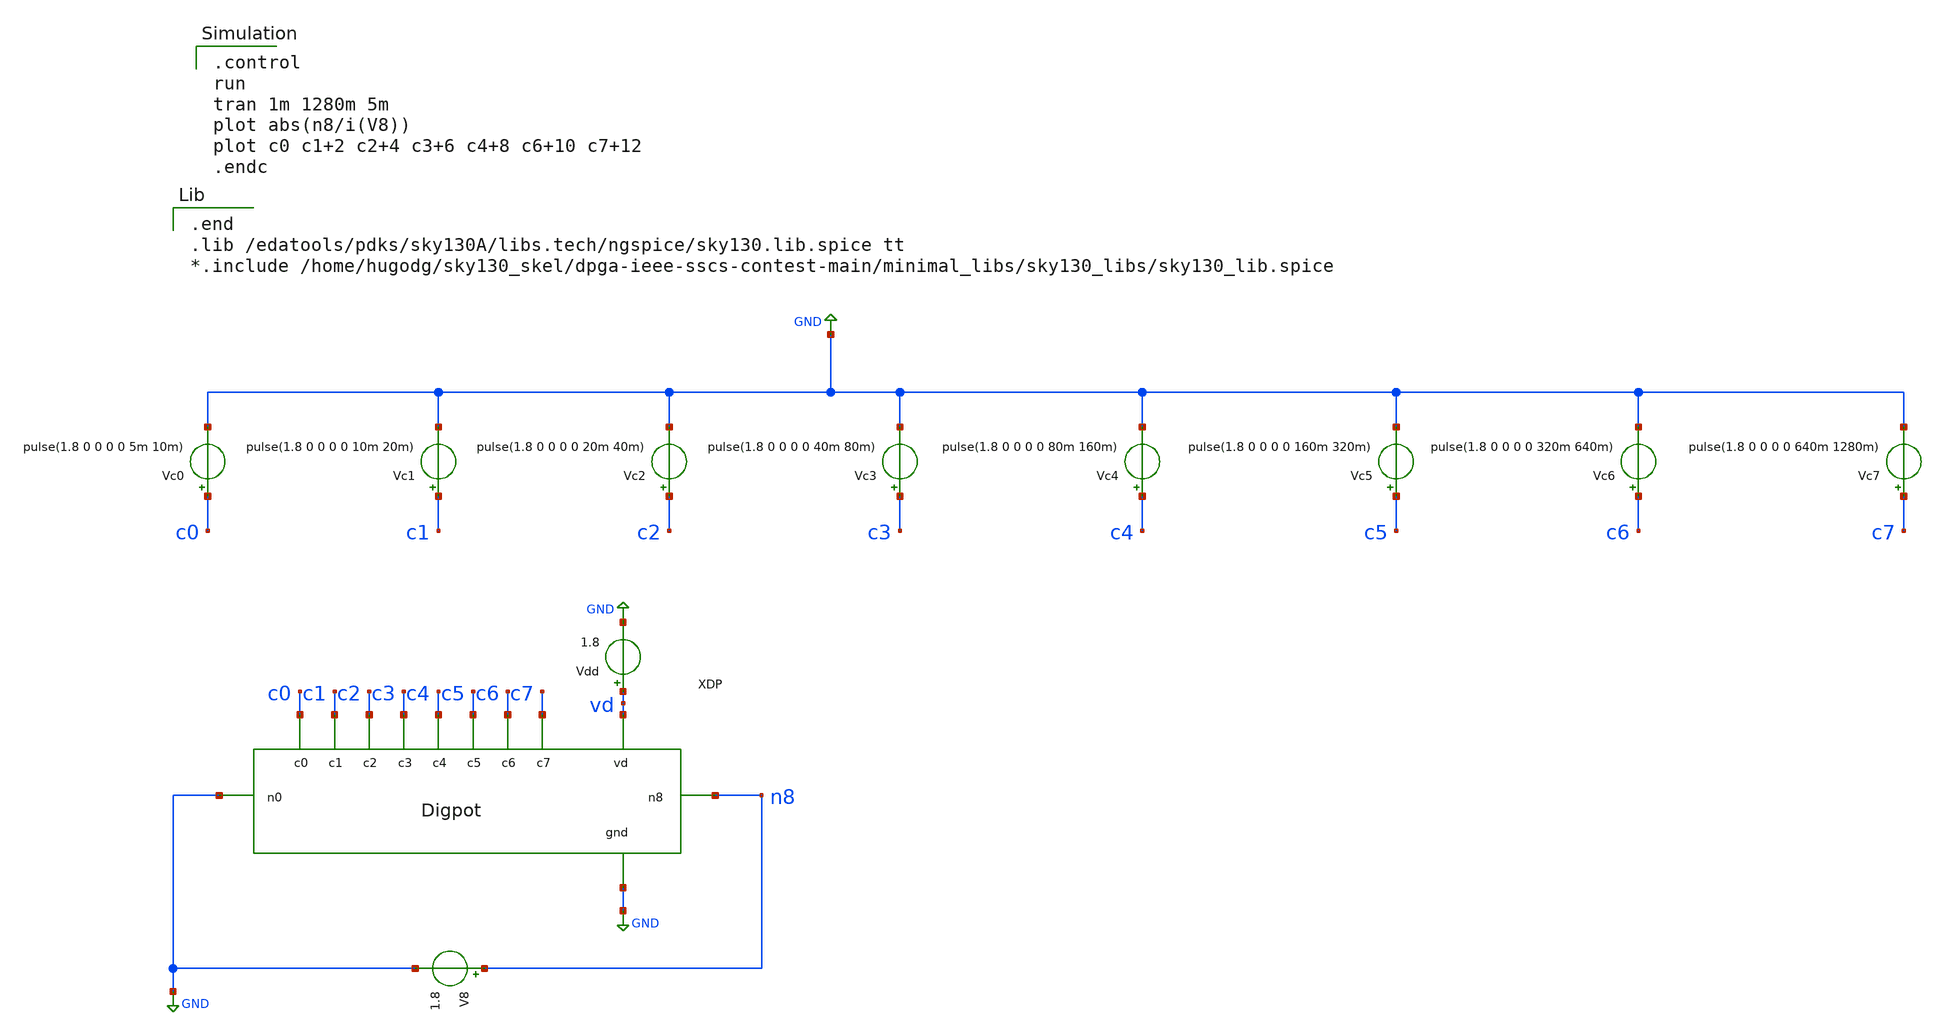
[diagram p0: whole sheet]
** sch_path: xschem/digpot-tb.sch
**.subckt digpot-tb
x1 GND vd c5 c1 c2 c6 c7 c3 c0 c4 n8 GND digpot
V8 n8 GND 1.8
Vdd vd GND 1.8
Vc0 c0 GND pulse(1.8 0 0 0 0 5m 10m)
Vc1 c1 GND pulse(1.8 0 0 0 0 10m 20m)
Vc2 c2 GND pulse(1.8 0 0 0 0 20m 40m)
Vc3 c3 GND pulse(1.8 0 0 0 0 40m 80m)
Vc4 c4 GND pulse(1.8 0 0 0 0 80m 160m)
Vc5 c5 GND pulse(1.8 0 0 0 0 160m 320m)
Vc6 c6 GND pulse(1.8 0 0 0 0 320m 640m)
Vc7 c7 GND pulse(1.8 0 0 0 0 640m 1280m)
**** begin user architecture code

.end
.lib /edatools/pdks/sky130A/libs.tech/ngspice/sky130.lib.spice tt
*.include /home/hugodg/sky130_skel/dpga-ieee-sscs-contest-main/minimal_libs/sky130_libs/sky130_lib.spice


.control
run
tran 1m 1280m 5m
plot abs(n8/i(V8))
plot c0 c1+2 c2+4 c3+6 c4+8 c6+10 c7+12
.endc

**** end user architecture code
**.ends

* expanding   symbol:  /home/hugodg/sky130_skel/dpga-ieee-sscs-contest-main/xschem/digpot.sym # of
*+ pins=12
** sym_path: xschem/digpot.sym
** sch_path: xschem/digpot.sch
.subckt digpot gnd vd c5 c1 c2 c6 c7 c3 c0 c4 n8 n0
*.ipin c0
*.ipin c1
*.ipin c2
*.ipin c3
*.ipin c4
*.ipin c5
*.ipin c6
*.ipin c7
*.iopin gnd
*.iopin vd
*.iopin n0
*.iopin n8
xtg1 c0 vd n1 gnd n0 tg
xtg2 c1 vd n2 gnd n1 tg
xtg3 c2 vd n3 gnd n2 tg
xtg4 c3 vd n4 gnd n3 tg
xtg5 c4 vd n5 gnd n4 tg
xtg6 c5 vd n6 gnd n5 tg
xtg7 c6 vd n7 gnd n6 tg
xtg8 c7 vd n8 gnd n7 tg
XR0 n1 n0 gnd sky130_fd_pr__res_high_po_0p35 L=0.98 mult=1 m=1
XR1 n2 n1 gnd sky130_fd_pr__res_high_po_0p35 L=2.07 mult=1 m=1
XR2 n3 n2 gnd sky130_fd_pr__res_xhigh_po_0p35 L=0.58 mult=1 m=1
XR3 n4 n3 gnd sky130_fd_pr__res_xhigh_po_0p35 L=1.28 mult=1 m=1
XR4 n5 n4 gnd sky130_fd_pr__res_xhigh_po_0p35 L=2.68 mult=1 m=1
XR5 n6 n5 gnd sky130_fd_pr__res_xhigh_po_0p35 L=5.48 mult=1 m=1
XR6 n7 n6 gnd sky130_fd_pr__res_xhigh_po_0p35 L=10.73 mult=1 m=1
XR7 n8 n7 gnd sky130_fd_pr__res_xhigh_po_0p35 L=22.28 mult=1 m=1
.ends


* expanding   symbol:  /home/hugodg/sky130_skel/dpga-ieee-sscs-contest-main/xschem/tg.sym # of
*+ pins=5
** sym_path: xschem/tg.sym
** sch_path: xschem/tg.sch
.subckt tg ctrl vd b vgnd a
*.iopin vd
*.iopin vgnd
*.iopin b
*.iopin a
*.ipin ctrl
XM2 a ctrl b b sky130_fd_pr__pfet_01v8 L=0.15 W=3 nf=1 ad='int((nf+1)/2) * W/nf * 0.29' as='int((nf+2)/2) * W/nf * 0.29'
+ pd='2*int((nf+1)/2) * (W/nf + 0.29)' ps='2*int((nf+2)/2) * (W/nf + 0.29)' nrd='0.29 / W' nrs='0.29 / W'
+ sa=0 sb=0 sd=0 mult=1 m=1
XM1 b nctrl net1 net1 sky130_fd_pr__nfet_01v8 L=0.15 W=1 nf=1 ad='int((nf+1)/2) * W/nf * 0.29' as='int((nf+2)/2) * W/nf * 0.29'
+ pd='2*int((nf+1)/2) * (W/nf + 0.29)' ps='2*int((nf+2)/2) * (W/nf + 0.29)' nrd='0.29 / W' nrs='0.29 / W'
+ sa=0 sb=0 sd=0 mult=1 m=1
XM3 nctrl ctrl vgnd vgnd sky130_fd_pr__nfet_01v8 L=0.15 W=1 nf=1 ad='int((nf+1)/2) * W/nf * 0.29' as='int((nf+2)/2) * W/nf * 0.29'
+ pd='2*int((nf+1)/2) * (W/nf + 0.29)' ps='2*int((nf+2)/2) * (W/nf + 0.29)' nrd='0.29 / W' nrs='0.29 / W'
+ sa=0 sb=0 sd=0 mult=1 m=1
XM4 nctrl ctrl vd vd sky130_fd_pr__pfet_01v8 L=0.15 W=3 nf=1 ad='int((nf+1)/2) * W/nf * 0.29' as='int((nf+2)/2) * W/nf * 0.29'
+ pd='2*int((nf+1)/2) * (W/nf + 0.29)' ps='2*int((nf+2)/2) * (W/nf + 0.29)' nrd='0.29 / W' nrs='0.29 / W'
+ sa=0 sb=0 sd=0 mult=1 m=1
.ends

.GLOBAL GND
.end
